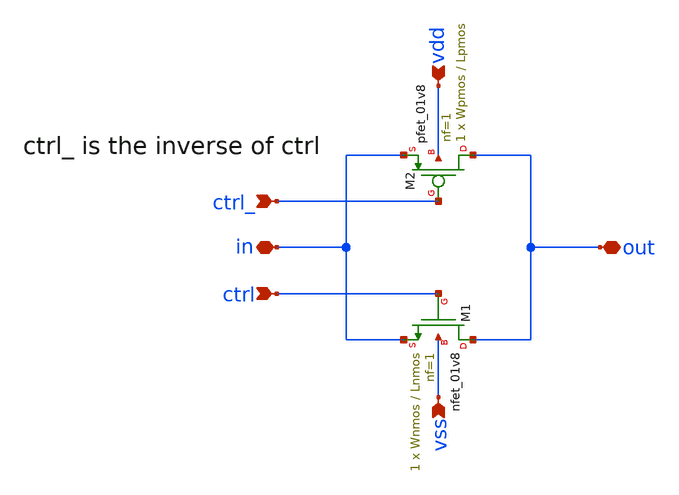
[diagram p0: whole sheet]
** sch_path: xschem/transmission_gate/transmission_gate.sch
**.subckt transmission_gate in out ctrl_ ctrl vdd vss
*.iopin in
*.iopin out
*.ipin ctrl_
*.ipin ctrl
*.ipin vdd
*.ipin vss
XM1 out ctrl in vss sky130_fd_pr__nfet_01v8 L=Lnmos W=Wnmos nf=1 ad='int((nf+1)/2) * W/nf * 0.29' as='int((nf+2)/2) * W/nf * 0.29'
+ pd='2*int((nf+1)/2) * (W/nf + 0.29)' ps='2*int((nf+2)/2) * (W/nf + 0.29)' nrd='0.29 / W' nrs='0.29 / W'
+ sa=0 sb=0 sd=0 mult=1 m=1
XM2 out ctrl_ in vdd sky130_fd_pr__pfet_01v8 L=Lpmos W=Wpmos nf=1 ad='int((nf+1)/2) * W/nf * 0.29' as='int((nf+2)/2) * W/nf * 0.29'
+ pd='2*int((nf+1)/2) * (W/nf + 0.29)' ps='2*int((nf+2)/2) * (W/nf + 0.29)' nrd='0.29 / W' nrs='0.29 / W'
+ sa=0 sb=0 sd=0 mult=1 m=1
**.ends
.end
